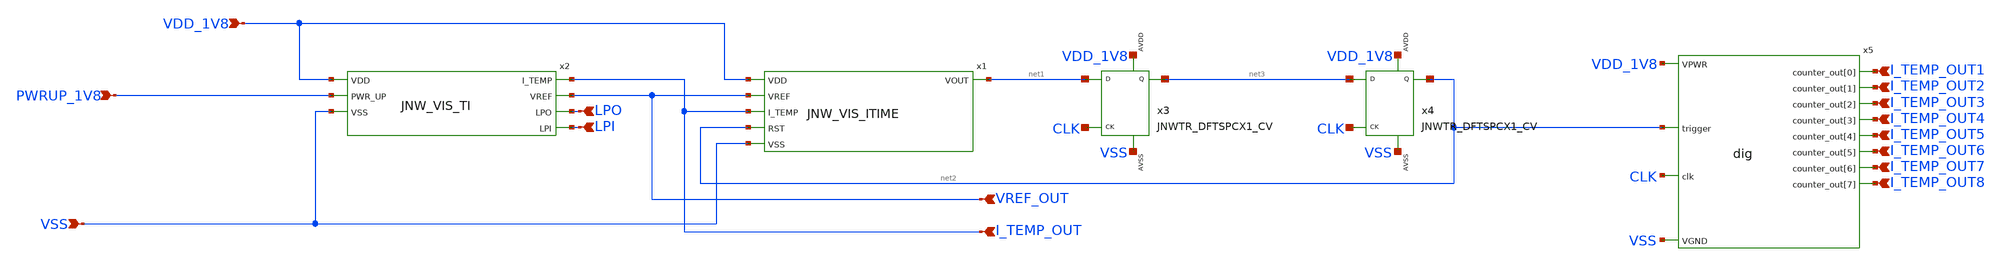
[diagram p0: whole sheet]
** sch_path: design/JNW_GR02_SKY130A/JNW_GR02_dig.sch
**.subckt JNW_GR02_dig VDD_1V8 VSS PWRUP_1V8 I_TEMP_OUT LPI LPO VREF_OUT I_TEMP_OUT8 I_TEMP_OUT7
*+ I_TEMP_OUT6 I_TEMP_OUT5 I_TEMP_OUT4 I_TEMP_OUT3 I_TEMP_OUT2 I_TEMP_OUT1
*.ipin VDD_1V8
*.ipin VSS
*.ipin PWRUP_1V8
*.ipin I_TEMP_OUT
*.ipin LPI
*.ipin LPO
*.ipin VREF_OUT
*.ipin I_TEMP_OUT8
*.ipin I_TEMP_OUT7
*.ipin I_TEMP_OUT6
*.ipin I_TEMP_OUT5
*.ipin I_TEMP_OUT4
*.ipin I_TEMP_OUT3
*.ipin I_TEMP_OUT2
*.ipin I_TEMP_OUT1
x1 VDD_1V8 VREF_OUT net1 I_TEMP_OUT net2 VSS JNW_VIS_ITIME
x2 I_TEMP_OUT VDD_1V8 VREF_OUT LPO LPI PWRUP_1V8 VSS JNW_VIS_TI
x3 net1 CLK net3 VDD_1V8 VSS JNWTR_DFTSPCX1_CV xoffset=0 yoffset=0 angle=0
x4 net3 CLK net2 VDD_1V8 VSS JNWTR_DFTSPCX1_CV xoffset=0 yoffset=0 angle=0
x5 VSS VDD_1V8 CLK I_TEMP_OUT1 I_TEMP_OUT2 I_TEMP_OUT3 I_TEMP_OUT4 I_TEMP_OUT5 I_TEMP_OUT6
+ I_TEMP_OUT7 I_TEMP_OUT8 net2 dig
**** begin user architecture code



.include /home/georg/aicex/ip/jnw_gr02_sky130a/design/JNW_GR02_SKY130A/dig.spice




**** end user architecture code
**.ends
.end
